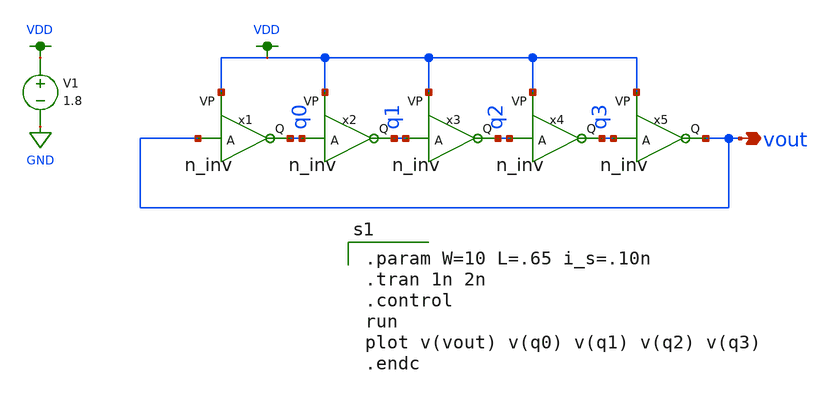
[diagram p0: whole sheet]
** sch_path: schemas/inv_testbench.sch
**.subckt inv_testbench vout
*.opin vout
x1 VDD q0 vout n_inv
x2 VDD q1 q0 n_inv
x3 VDD q2 q1 n_inv
x4 VDD q3 q2 n_inv
x5 VDD vout q3 n_inv
V1 VDD GND 1.8
**** begin user architecture code

.option wnflag=1
.lib ~/skywater/skywater-pdk/libraries/sky130_fd_pr_ngspice/latest/models/sky130.lib.spice tt


.param W=10 L=.65 i_s=.10n
.tran 1n 2n
.control
run
plot v(vout) v(q0) v(q1) v(q2) v(q3)
.endc


**** end user architecture code
**.ends

* expanding   symbol:  /home/lxbtlr/DTILO/schemas/n_inv.sym # of pins=3
** sym_path: schemas/n_inv.sym
** sch_path: schemas/n_inv.sch
.subckt n_inv VP Q A
*.ipin A
*.ipin VP
*.opin Q
XM1 Q A GND GND sky130_fd_pr__nfet_01v8 L={L} W={W} nf=1 ad='int((nf+1)/2) * W/nf * 0.29' as='int((nf+2)/2) * W/nf * 0.29'
+ pd='2*int((nf+1)/2) * (W/nf + 0.29)' ps='2*int((nf+2)/2) * (W/nf + 0.29)' nrd='0.29 / W' nrs='0.29 / W'
+ sa=0 sb=0 sd=0 mult=1 m=1
XM2 Q A VP VDD sky130_fd_pr__pfet_01v8 L={L} W={W} nf=1 ad='int((nf+1)/2) * W/nf * 0.29' as='int((nf+2)/2) * W/nf * 0.29'
+ pd='2*int((nf+1)/2) * (W/nf + 0.29)' ps='2*int((nf+2)/2) * (W/nf + 0.29)' nrd='0.29 / W' nrs='0.29 / W'
+ sa=0 sb=0 sd=0 mult=2 m=2
.ends

.GLOBAL VDD
.GLOBAL GND
.end
